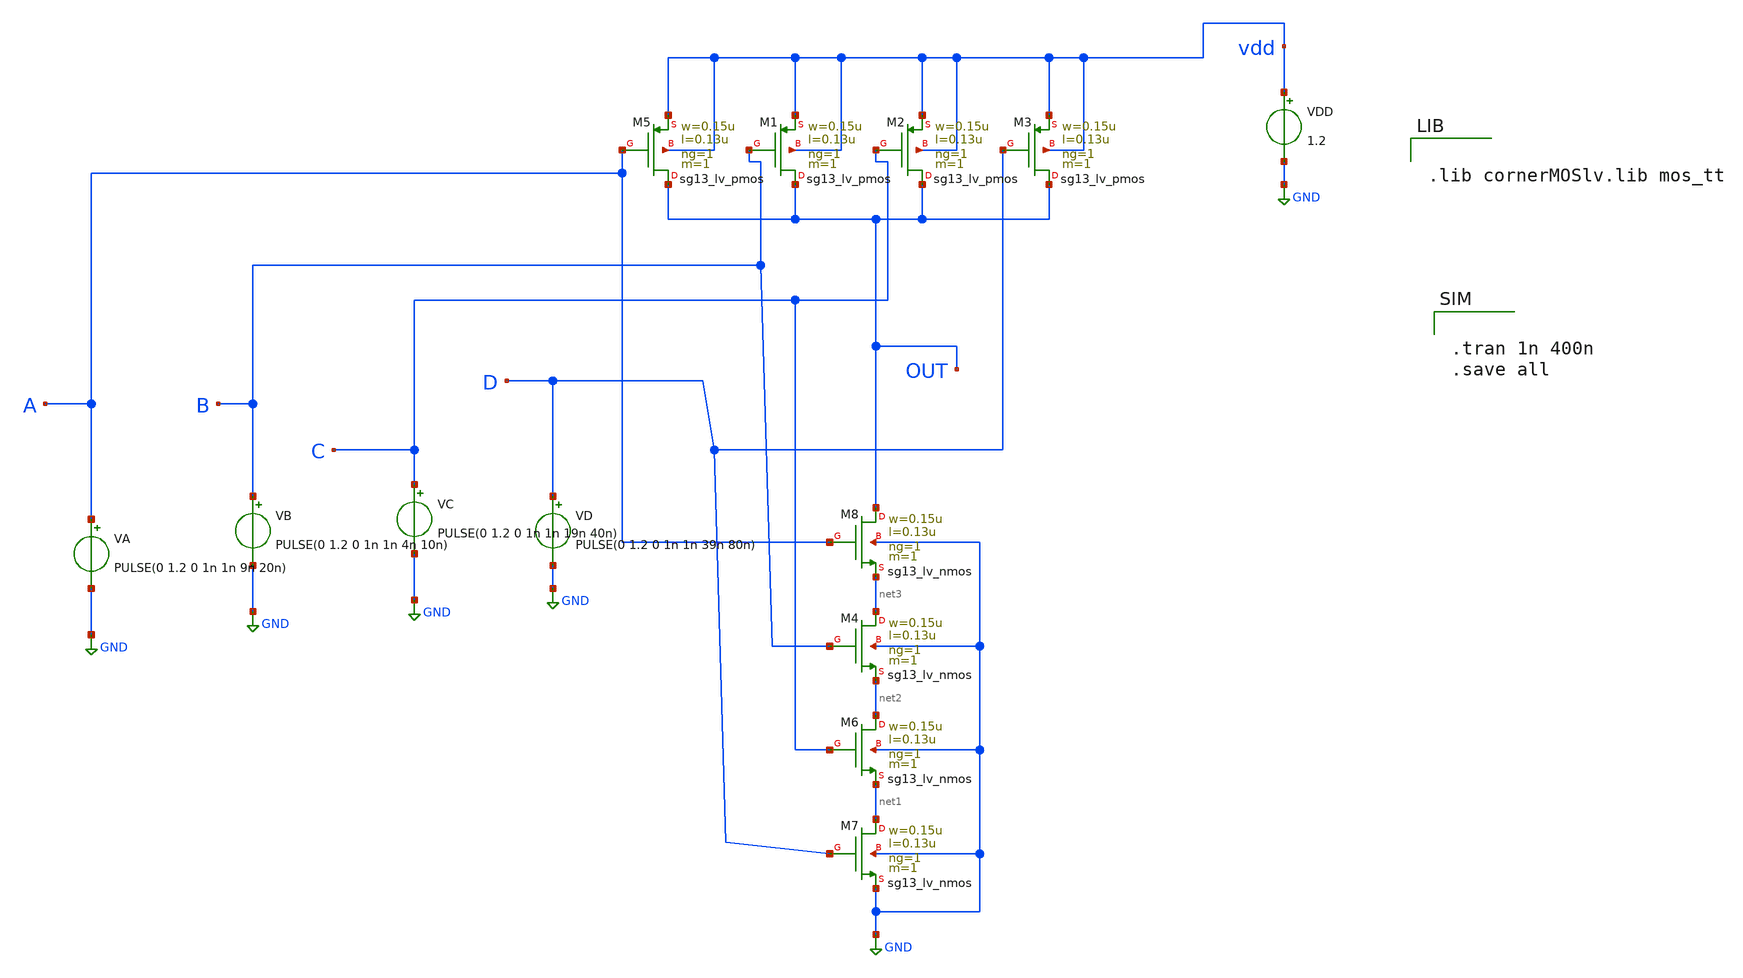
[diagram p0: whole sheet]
** sch_path: nand4.sch
**.subckt nand4
VA A GND PULSE(0 1.2 0 1n 1n 9n 20n)
VB B GND PULSE(0 1.2 0 1n 1n 4n 10n)
VC C GND PULSE(0 1.2 0 1n 1n 19n 40n)
VD D GND PULSE(0 1.2 0 1n 1n 39n 80n)
VDD vdd GND 1.2
XM5 OUT A vdd vdd sg13_lv_pmos w=0.15u l=0.13u ng=1 m=1 mm_ok=1
XM1 OUT B vdd vdd sg13_lv_pmos w=0.15u l=0.13u ng=1 m=1 mm_ok=1
XM2 OUT C vdd vdd sg13_lv_pmos w=0.15u l=0.13u ng=1 m=1 mm_ok=1
XM3 OUT D vdd vdd sg13_lv_pmos w=0.15u l=0.13u ng=1 m=1 mm_ok=1
XM8 OUT A net3 GND sg13_lv_nmos w=0.15u l=0.13u ng=1 m=1 mm_ok=1
XM4 net3 B net2 GND sg13_lv_nmos w=0.15u l=0.13u ng=1 m=1 mm_ok=1
XM6 net2 C net1 GND sg13_lv_nmos w=0.15u l=0.13u ng=1 m=1 mm_ok=1
XM7 net1 D GND GND sg13_lv_nmos w=0.15u l=0.13u ng=1 m=1 mm_ok=1
**** begin user architecture code


.lib cornerMOSlv.lib mos_tt



.tran 1n 400n
.save all


**** end user architecture code
**.ends
.GLOBAL GND
.end
